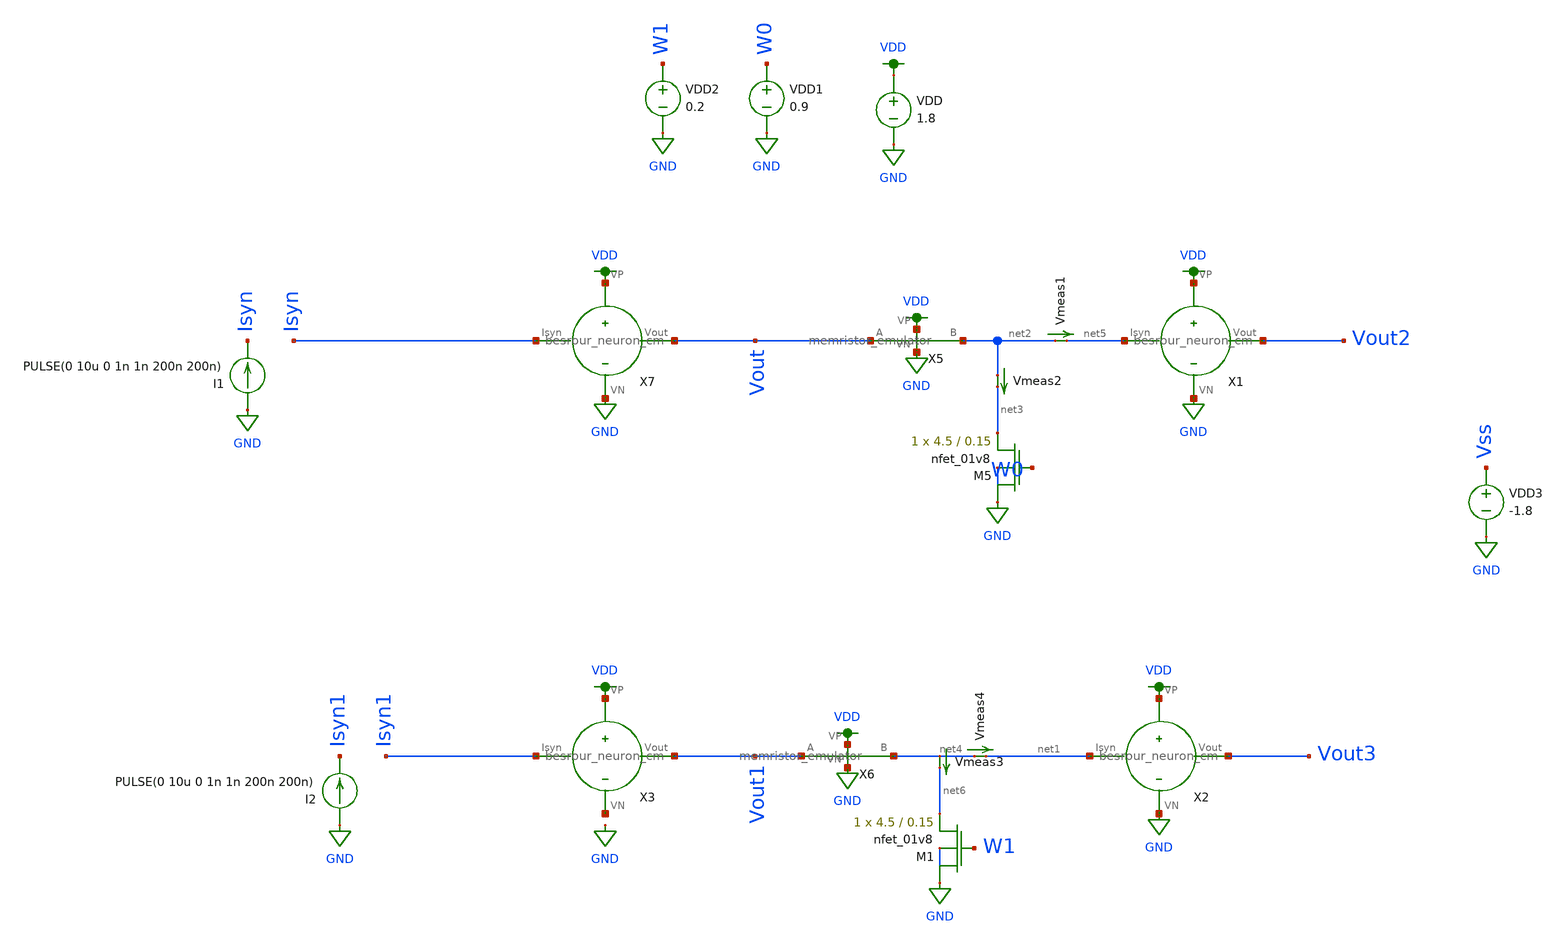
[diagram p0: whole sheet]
** sch_path: schematic/tran_besrour_mem.sch
**.subckt tran_besrour_mem
VDD VDD GND 1.8
VDD1 W0 GND 0.9
VDD2 W1 GND 0.2
I1 GND Isyn PULSE(0 10u 0 1n 1n 200n 200n)
I2 GND Isyn1 PULSE(0 10u 0 1n 1n 200n 200n)
Vmeas2 net2 net3 0
.save i(vmeas2)
XM5 GND W0 net3 GND sky130_fd_pr__nfet_01v8 L=0.15 W=4.5 nf=1 ad='int((nf+1)/2) * W/nf * 0.29' as='int((nf+2)/2) * W/nf * 0.29'
+ pd='2*int((nf+1)/2) * (W/nf + 0.29)' ps='2*int((nf+2)/2) * (W/nf + 0.29)' nrd='0.29 / W' nrs='0.29 / W'
+ sa=0 sb=0 sd=0 mult=1 m=1
X5 VDD GND net2 Vout memristor_emulator
X6 VDD GND net4 Vout1 memristor_emulator
X7 Isyn Vout VDD GND besrour_neuron_cm
X1 net5 Vout2 VDD GND besrour_neuron_cm
X2 net1 Vout3 VDD GND besrour_neuron_cm
X3 Isyn1 Vout1 VDD net7 besrour_neuron_cm
Vmeas1 net2 net5 0
.save i(vmeas1)
Vmeas4 net4 net1 0
.save i(vmeas4)
Vmeas3 net4 net6 0
.save i(vmeas3)
XM1 GND W1 net6 GND sky130_fd_pr__nfet_01v8 L=0.15 W=4.5 nf=1 ad='int((nf+1)/2) * W/nf * 0.29' as='int((nf+2)/2) * W/nf * 0.29'
+ pd='2*int((nf+1)/2) * (W/nf + 0.29)' ps='2*int((nf+2)/2) * (W/nf + 0.29)' nrd='0.29 / W' nrs='0.29 / W'
+ sa=0 sb=0 sd=0 mult=1 m=1
VDD3 Vss GND -1.8
**** begin user architecture code

.param W=1
.param L=0.15
.tran 0.1n 500n
.save all


.option wnflag=1
.param MC_SWITCH=0.0
.lib ~/skywater/skywater-pdk/libraries/sky130_fd_pr_ngspice/latest/models/sky130.lib.spice tt

**** end user architecture code
**.ends

* expanding   symbol:  /home/madvlsi/neuromorphic_computing_final/schematic/memristor_emulator.sym #
*+ of pins=4
** sym_path: schematic/memristor_emulator.sym
** sch_path: schematic/memristor_emulator.sch
.subckt memristor_emulator VP VN B A
*.ipin A
*.iopin VN
*.iopin VP
*.opin B
XM1 B in_cap A B sky130_fd_pr__pfet_01v8 L=0.3 W=12 nf=1 ad='int((nf+1)/2) * W/nf * 0.29' as='int((nf+2)/2) * W/nf * 0.29'
+ pd='2*int((nf+1)/2) * (W/nf + 0.29)' ps='2*int((nf+2)/2) * (W/nf + 0.29)' nrd='0.29 / W' nrs='0.29 / W'
+ sa=0 sb=0 sd=0 mult=1 m=1
XM2 VP A in_cap VP sky130_fd_pr__pfet_01v8 L=2 W=3 nf=1 ad='int((nf+1)/2) * W/nf * 0.29' as='int((nf+2)/2) * W/nf * 0.29'
+ pd='2*int((nf+1)/2) * (W/nf + 0.29)' ps='2*int((nf+2)/2) * (W/nf + 0.29)' nrd='0.29 / W' nrs='0.29 / W'
+ sa=0 sb=0 sd=0 mult=1 m=1
XM3 VN in_cap VN VN sky130_fd_pr__nfet_01v8 L=20 W=20 nf=1 ad='int((nf+1)/2) * W/nf * 0.29' as='int((nf+2)/2) * W/nf * 0.29'
+ pd='2*int((nf+1)/2) * (W/nf + 0.29)' ps='2*int((nf+2)/2) * (W/nf + 0.29)' nrd='0.29 / W' nrs='0.29 / W'
+ sa=0 sb=0 sd=0 mult=1 m=1
XM4 VN B in_cap VN sky130_fd_pr__nfet_01v8 L=3 W=2 nf=1 ad='int((nf+1)/2) * W/nf * 0.29' as='int((nf+2)/2) * W/nf * 0.29'
+ pd='2*int((nf+1)/2) * (W/nf + 0.29)' ps='2*int((nf+2)/2) * (W/nf + 0.29)' nrd='0.29 / W' nrs='0.29 / W'
+ sa=0 sb=0 sd=0 mult=1 m=1
.ends


* expanding   symbol:  /home/madvlsi/neuromorphic_computing_final/schematic/besrour_neuron_cm.sym #
*+ of pins=4
** sym_path: schematic/besrour_neuron_cm.sym
** sch_path: schematic/besrour_neuron_cm.sch
.subckt besrour_neuron_cm Isyn Vout VP VN
*.iopin VP
*.iopin VN
*.iopin Isyn
*.opin Vout
XM2 VMEMINT net1 VP VDD sky130_fd_pr__pfet_01v8 L={L} W={W} nf=1 ad='int((nf+1)/2) * W/nf * 0.29' as='int((nf+2)/2) * W/nf * 0.29'
+ pd='2*int((nf+1)/2) * (W/nf + 0.29)' ps='2*int((nf+2)/2) * (W/nf + 0.29)' nrd='0.29 / W' nrs='0.29 / W'
+ sa=0 sb=0 sd=0 mult=1 m=1
XM3 VP net3 VMEMINT VDD sky130_fd_pr__pfet_01v8 L={L} W={W} nf=1 ad='int((nf+1)/2) * W/nf * 0.29' as='int((nf+2)/2) * W/nf * 0.29'
+ pd='2*int((nf+1)/2) * (W/nf + 0.29)' ps='2*int((nf+2)/2) * (W/nf + 0.29)' nrd='0.29 / W' nrs='0.29 / W'
+ sa=0 sb=0 sd=0 mult=1 m=1
XM4 net3 VMEMINT VP VDD sky130_fd_pr__pfet_01v8 L={L} W={W} nf=1 ad='int((nf+1)/2) * W/nf * 0.29' as='int((nf+2)/2) * W/nf * 0.29'
+ pd='2*int((nf+1)/2) * (W/nf + 0.29)' ps='2*int((nf+2)/2) * (W/nf + 0.29)' nrd='0.29 / W' nrs='0.29 / W'
+ sa=0 sb=0 sd=0 mult=1 m=1
XM5 net2 net3 VP VDD sky130_fd_pr__pfet_01v8 L={L} W={W} nf=1 ad='int((nf+1)/2) * W/nf * 0.29' as='int((nf+2)/2) * W/nf * 0.29'
+ pd='2*int((nf+1)/2) * (W/nf + 0.29)' ps='2*int((nf+2)/2) * (W/nf + 0.29)' nrd='0.29 / W' nrs='0.29 / W'
+ sa=0 sb=0 sd=0 mult=1 m=1
XM6 net3 VMEMINT VN GND sky130_fd_pr__nfet_01v8 L={L} W={W} nf=1 ad='int((nf+1)/2) * W/nf * 0.29' as='int((nf+2)/2) * W/nf * 0.29'
+ pd='2*int((nf+1)/2) * (W/nf + 0.29)' ps='2*int((nf+2)/2) * (W/nf + 0.29)' nrd='0.29 / W' nrs='0.29 / W'
+ sa=0 sb=0 sd=0 mult=1 m=1
XM8 net2 net3 VN GND sky130_fd_pr__nfet_01v8 L={L} W={W} nf=1 ad='int((nf+1)/2) * W/nf * 0.29' as='int((nf+2)/2) * W/nf * 0.29'
+ pd='2*int((nf+1)/2) * (W/nf + 0.29)' ps='2*int((nf+2)/2) * (W/nf + 0.29)' nrd='0.29 / W' nrs='0.29 / W'
+ sa=0 sb=0 sd=0 mult=1 m=1
C1 VMEMINT VN 340f m=1
C2 net2 VN 340f m=1
XM9 net4 net2 VP VDD sky130_fd_pr__pfet_01v8 L={L} W={W} nf=1 ad='int((nf+1)/2) * W/nf * 0.29' as='int((nf+2)/2) * W/nf * 0.29'
+ pd='2*int((nf+1)/2) * (W/nf + 0.29)' ps='2*int((nf+2)/2) * (W/nf + 0.29)' nrd='0.29 / W' nrs='0.29 / W'
+ sa=0 sb=0 sd=0 mult=1 m=1
XM10 net4 net2 VN GND sky130_fd_pr__nfet_01v8 L={L} W={W} nf=1 ad='int((nf+1)/2) * W/nf * 0.29' as='int((nf+2)/2) * W/nf * 0.29'
+ pd='2*int((nf+1)/2) * (W/nf + 0.29)' ps='2*int((nf+2)/2) * (W/nf + 0.29)' nrd='0.29 / W' nrs='0.29 / W'
+ sa=0 sb=0 sd=0 mult=1 m=1
XM11 Vout net4 VP VDD sky130_fd_pr__pfet_01v8 L={L} W={W} nf=1 ad='int((nf+1)/2) * W/nf * 0.29' as='int((nf+2)/2) * W/nf * 0.29'
+ pd='2*int((nf+1)/2) * (W/nf + 0.29)' ps='2*int((nf+2)/2) * (W/nf + 0.29)' nrd='0.29 / W' nrs='0.29 / W'
+ sa=0 sb=0 sd=0 mult=1 m=1
XM12 Vout net4 VN GND sky130_fd_pr__nfet_01v8 L={L} W={W} nf=1 ad='int((nf+1)/2) * W/nf * 0.29' as='int((nf+2)/2) * W/nf * 0.29'
+ pd='2*int((nf+1)/2) * (W/nf + 0.29)' ps='2*int((nf+2)/2) * (W/nf + 0.29)' nrd='0.29 / W' nrs='0.29 / W'
+ sa=0 sb=0 sd=0 mult=1 m=1
XM13 net1 Isyn VN GND sky130_fd_pr__nfet_01v8 L={L} W={W} nf=1 ad='int((nf+1)/2) * W/nf * 0.29' as='int((nf+2)/2) * W/nf * 0.29'
+ pd='2*int((nf+1)/2) * (W/nf + 0.29)' ps='2*int((nf+2)/2) * (W/nf + 0.29)' nrd='0.29 / W' nrs='0.29 / W'
+ sa=0 sb=0 sd=0 mult=1 m=1
XM14 VN Isyn Isyn GND sky130_fd_pr__nfet_01v8 L={L} W={W} nf=1 ad='int((nf+1)/2) * W/nf * 0.29' as='int((nf+2)/2) * W/nf * 0.29'
+ pd='2*int((nf+1)/2) * (W/nf + 0.29)' ps='2*int((nf+2)/2) * (W/nf + 0.29)' nrd='0.29 / W' nrs='0.29 / W'
+ sa=0 sb=0 sd=0 mult=1 m=1
XM1 VP net1 net1 VDD sky130_fd_pr__pfet_01v8 L={L} W={W} nf=1 ad='int((nf+1)/2) * W/nf * 0.29' as='int((nf+2)/2) * W/nf * 0.29'
+ pd='2*int((nf+1)/2) * (W/nf + 0.29)' ps='2*int((nf+2)/2) * (W/nf + 0.29)' nrd='0.29 / W' nrs='0.29 / W'
+ sa=0 sb=0 sd=0 mult=1 m=1
XM7 VN net2 VMEMINT GND sky130_fd_pr__nfet_01v8 L={L} W={W} nf=1 ad='int((nf+1)/2) * W/nf * 0.29' as='int((nf+2)/2) * W/nf * 0.29'
+ pd='2*int((nf+1)/2) * (W/nf + 0.29)' ps='2*int((nf+2)/2) * (W/nf + 0.29)' nrd='0.29 / W' nrs='0.29 / W'
+ sa=0 sb=0 sd=0 mult=1 m=1
.ends

.GLOBAL VDD
.GLOBAL GND
.end
